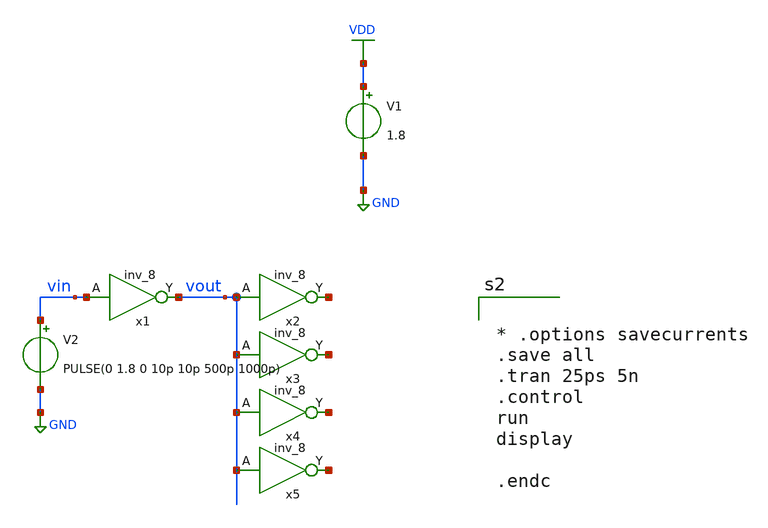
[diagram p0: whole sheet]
** sch_path: xschem/test.sch
**.subckt test
x1 vin gnd gnd vdd vdd vout sky130_fd_sc_hd__inv_8
V1 VDD GND 1.8
V2 vin GND PULSE(0 1.8 0 10p 10p 500p 1000p)
x2 vout gnd gnd vdd vdd net1 sky130_fd_sc_hd__inv_8
x3 vout gnd gnd vdd vdd net2 sky130_fd_sc_hd__inv_8
x4 vout gnd gnd vdd vdd net3 sky130_fd_sc_hd__inv_8
x5 vout gnd gnd vdd vdd net4 sky130_fd_sc_hd__inv_8
**** begin user architecture code
.lib $::SKYWATER_MODELS/sky130.lib.spice tt
.include $::PDKPATH/libs.ref/sky130_fd_sc_hd/spice/sky130_fd_sc_hd.spice



* .options savecurrents
.save all
.tran 25ps 5n
.control
run
display

.endc


**** end user architecture code
**.ends
.GLOBAL VDD
.GLOBAL GND
.end
